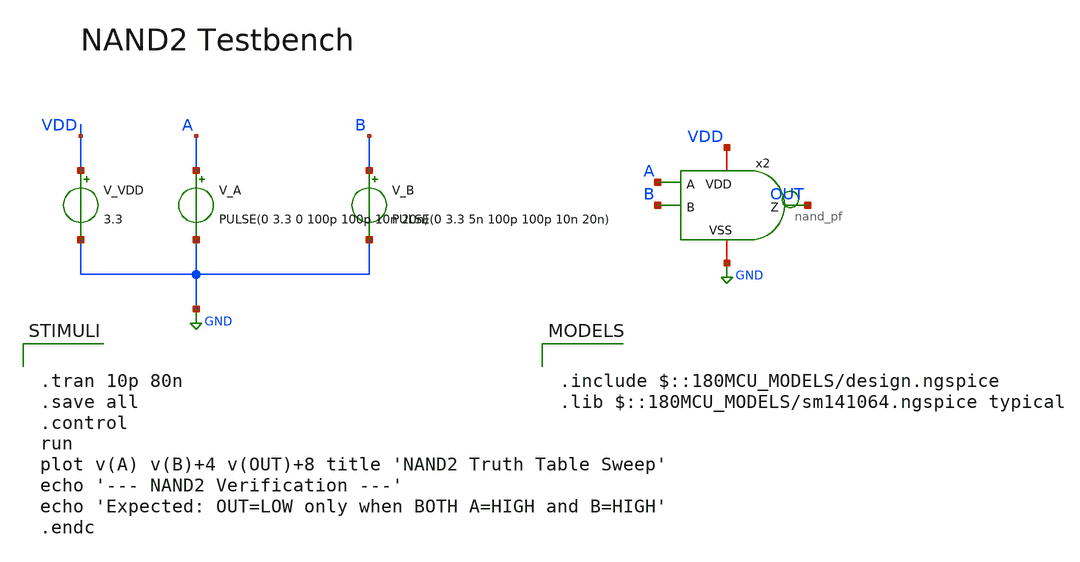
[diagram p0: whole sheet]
** sch_path: designs/libs/PDF/nand_pf_tb.sch
**.subckt nand_pf_tb
V_A A GND PULSE(0 3.3 0 100p 100p 10n 20n)
V_B B GND PULSE(0 3.3 5n 100p 100p 10n 20n)
V_VDD VDD GND 3.3
x2 VDD OUT A B GND nand_pf
**** begin user architecture code


.tran 10p 80n
.save all
.control
run
plot v(A) v(B)+4 v(OUT)+8 title 'NAND2 Truth Table Sweep'
echo '--- NAND2 Verification ---'
echo 'Expected: OUT=LOW only when BOTH A=HIGH and B=HIGH'
.endc



.include $::180MCU_MODELS/design.ngspice
.lib $::180MCU_MODELS/sm141064.ngspice typical

**** end user architecture code
**.ends
.GLOBAL GND
.end
